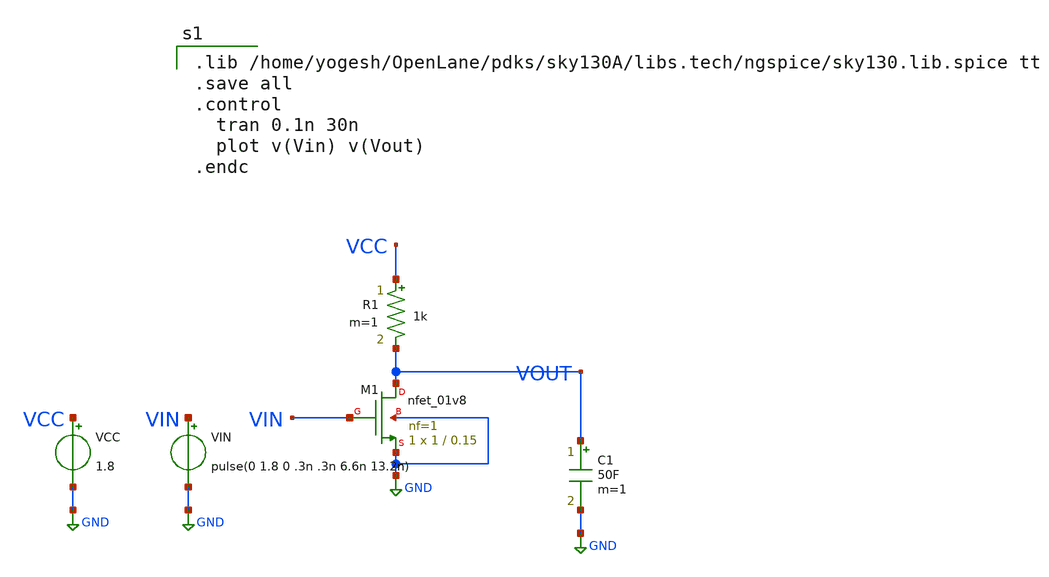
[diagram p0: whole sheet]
** sch_path: OneDrive/Documents/CMOS-Inverter-Design-and-Analysis-using-Sky130pdk-main/xschem/nmos_invF.sch
**.subckt nmos_invF
XM1 VOUT VIN GND GND sky130_fd_pr__nfet_01v8 L=0.15 W=1 nf=1 ad='int((nf+1)/2) * W/nf * 0.29' as='int((nf+2)/2) * W/nf * 0.29'
+ pd='2*int((nf+1)/2) * (W/nf + 0.29)' ps='2*int((nf+2)/2) * (W/nf + 0.29)' nrd='0.29 / W' nrs='0.29 / W'
+ sa=0 sb=0 sd=0 mult=1 m=1
VIN VIN GND pulse(0 1.8 0 .3n .3n 6.6n 13.2n)
VCC VCC GND 1.8
R1 VCC VOUT 1k m=1
C1 VOUT GND 50F m=1
**** begin user architecture code

.lib /home/yogesh/OpenLane/pdks/sky130A/libs.tech/ngspice/sky130.lib.spice tt
.save all
.control
  tran 0.1n 30n
  plot v(Vin) v(Vout)
.endc

**** end user architecture code
**.ends
.GLOBAL GND
.end
